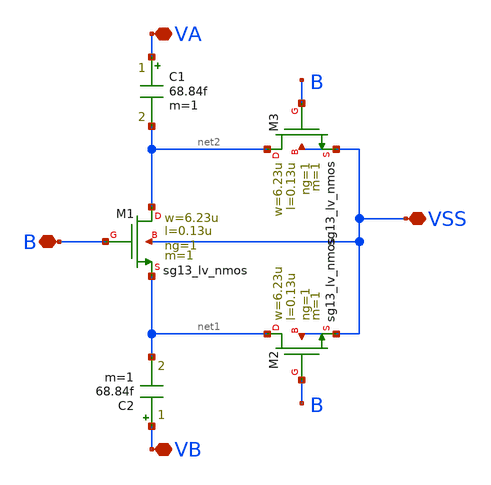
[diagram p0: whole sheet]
** sch_path: analog/core/cap_bank_unit.sch
**.subckt cap_bank_unit VA VSS B VB
*.iopin VA
*.iopin VSS
*.iopin B
*.iopin VB
C1 VA net2 68.84f m=1
C2 VB net1 68.84f m=1
XM1 net2 B net1 VSS sg13_lv_nmos w=6.23u l=0.13u ng=1 m=1 mm_ok=1
XM2 net1 B VSS VSS sg13_lv_nmos w=6.23u l=0.13u ng=1 m=1 mm_ok=1
XM3 net2 B VSS VSS sg13_lv_nmos w=6.23u l=0.13u ng=1 m=1 mm_ok=1
**.ends
.end
